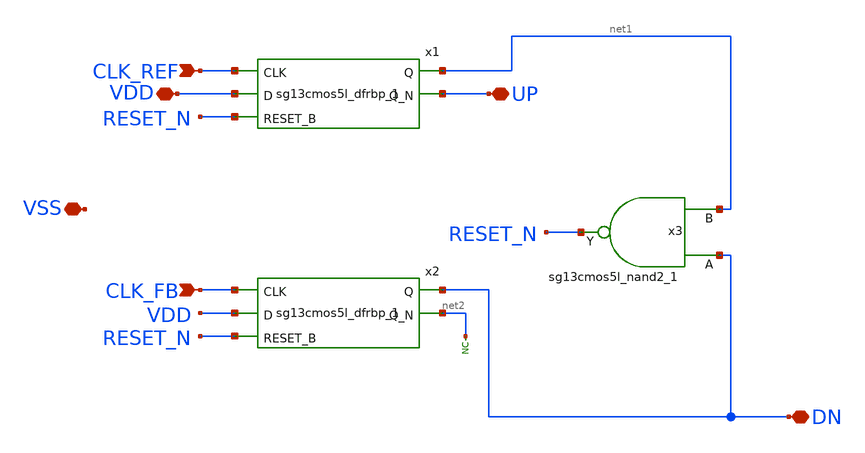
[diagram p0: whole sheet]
** sch_path: macros/heichips26_ook/macros/ook_analog_system/schematic/xschem/pfd.sch
**.subckt pfd VDD VSS CLK_REF CLK_FB DN UP
*.iopin VDD
*.iopin VSS
*.ipin CLK_REF
*.ipin CLK_FB
*.iopin DN
*.iopin UP
x1 net1 UP CLK_REF VDD RESET_N VDD VSS sg13cmos5l_dfrbp_1
x2 DN net2 CLK_FB VDD RESET_N VDD VSS sg13cmos5l_dfrbp_1
* noconn #net2
x3 RESET_N DN net1 VDD VSS sg13cmos5l_nand2_1
**.ends
.end
